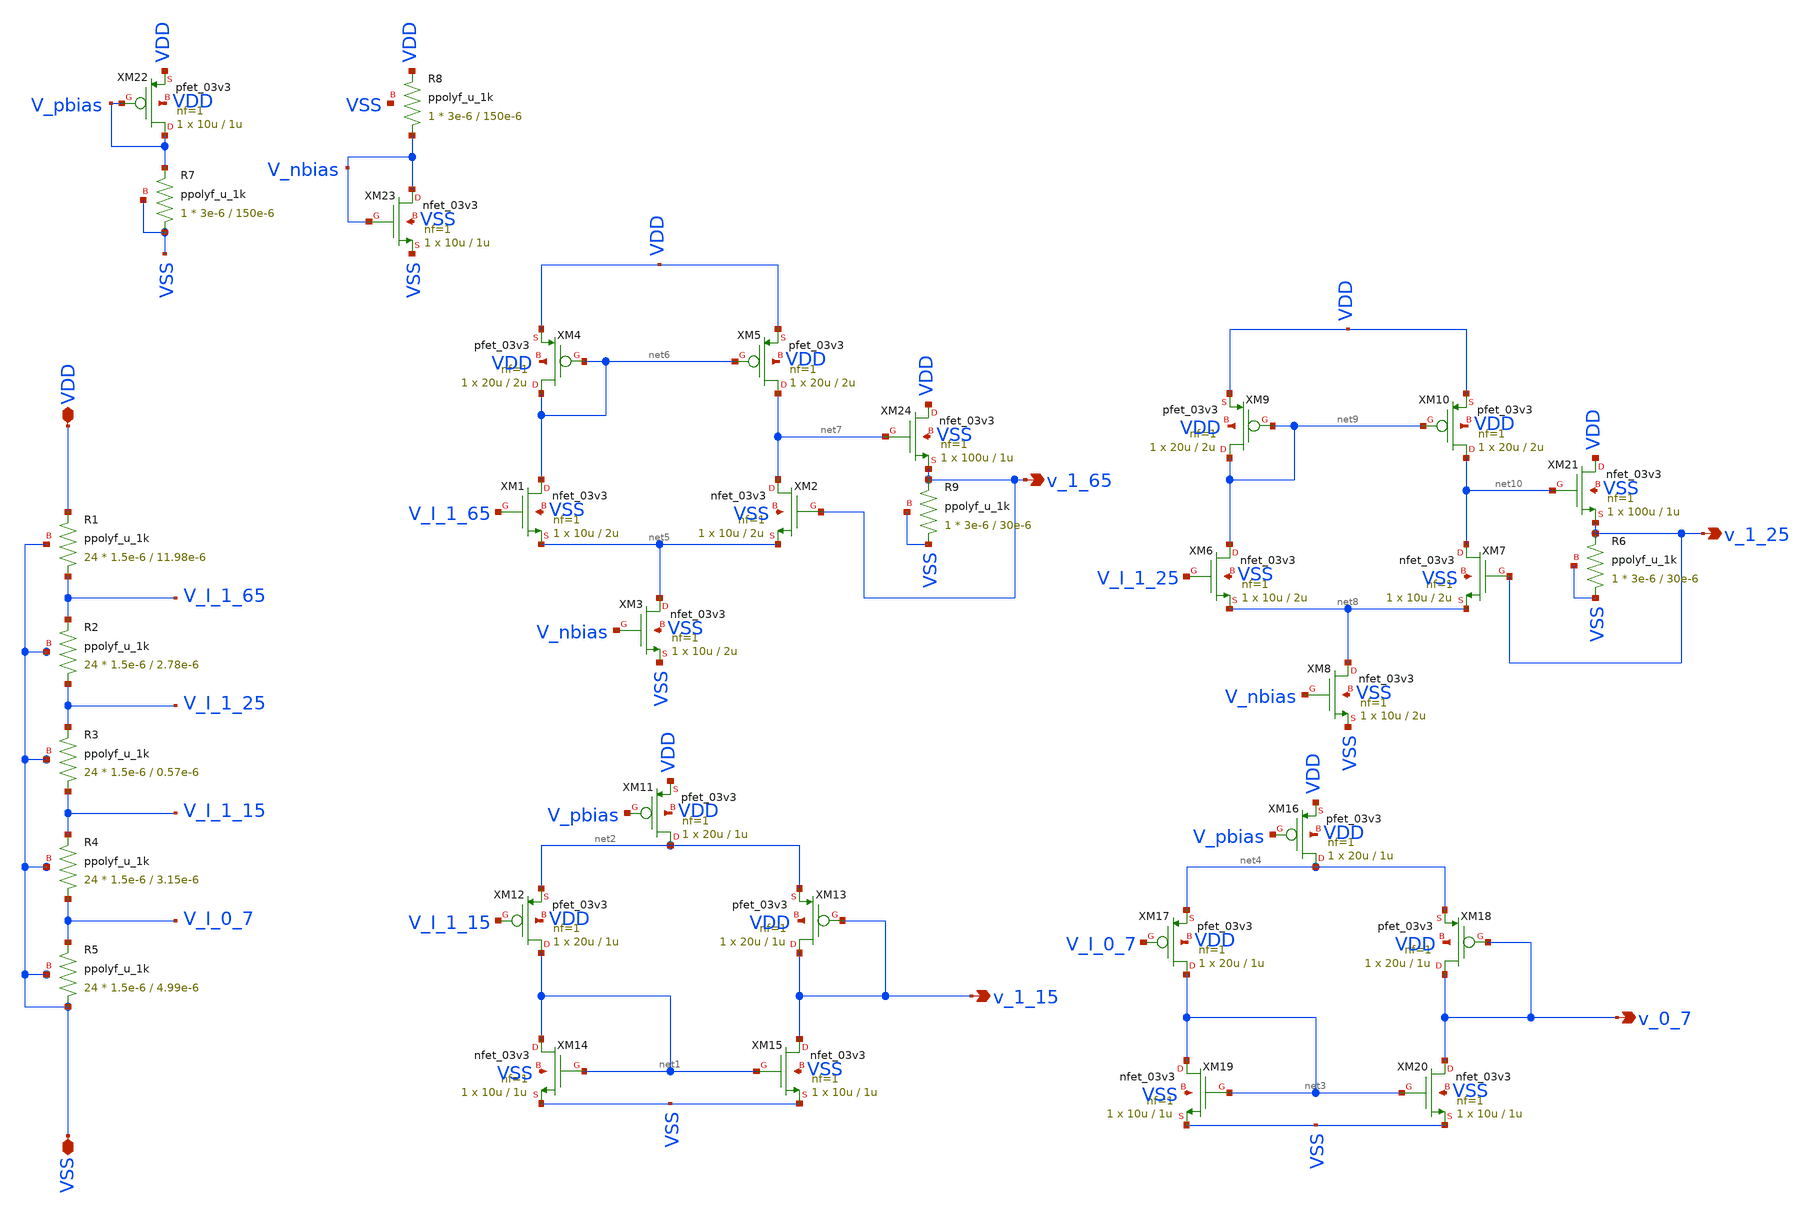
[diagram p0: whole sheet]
** sch_path: schematics/voltage_reference.sch
**.subckt voltage_reference VDD VSS v_1_65 v_1_15 v_0_7 v_1_25
*.iopin VDD
*.iopin VSS
*.opin v_1_65
*.opin v_1_15
*.opin v_0_7
*.opin v_1_25
XR1 V_I_1_65 VDD VSS ppolyf_u_1k r_width=1.5e-6 r_length=11.98e-6 m=24
XR2 V_I_1_25 V_I_1_65 VSS ppolyf_u_1k r_width=1.5e-6 r_length=2.78e-6 m=24
XR3 V_I_1_15 V_I_1_25 VSS ppolyf_u_1k r_width=1.5e-6 r_length=0.57e-6 m=24
XR4 V_I_0_7 V_I_1_15 VSS ppolyf_u_1k r_width=1.5e-6 r_length=3.15e-6 m=24
XR5 VSS V_I_0_7 VSS ppolyf_u_1k r_width=1.5e-6 r_length=4.99e-6 m=24
XM11 net2 V_pbias VDD VDD pfet_03v3 L=1u W=20u nf=1 ad='int((nf+1)/2) * W/nf * 0.18u' as='int((nf+2)/2) * W/nf * 0.18u'
+ pd='2*int((nf+1)/2) * (W/nf + 0.18u)' ps='2*int((nf+2)/2) * (W/nf + 0.18u)' nrd='0.18u / W' nrs='0.18u / W'
+ sa=0 sb=0 sd=0 m=1
XM12 net1 V_I_1_15 net2 VDD pfet_03v3 L=1u W=20u nf=1 ad='int((nf+1)/2) * W/nf * 0.18u' as='int((nf+2)/2) * W/nf * 0.18u'
+ pd='2*int((nf+1)/2) * (W/nf + 0.18u)' ps='2*int((nf+2)/2) * (W/nf + 0.18u)' nrd='0.18u / W' nrs='0.18u / W'
+ sa=0 sb=0 sd=0 m=1
XM13 v_1_15 v_1_15 net2 VDD pfet_03v3 L=1u W=20u nf=1 ad='int((nf+1)/2) * W/nf * 0.18u' as='int((nf+2)/2) * W/nf * 0.18u'
+ pd='2*int((nf+1)/2) * (W/nf + 0.18u)' ps='2*int((nf+2)/2) * (W/nf + 0.18u)' nrd='0.18u / W' nrs='0.18u / W'
+ sa=0 sb=0 sd=0 m=1
XM14 net1 net1 VSS VSS nfet_03v3 L=1u W=10u nf=1 ad='int((nf+1)/2) * W/nf * 0.18u' as='int((nf+2)/2) * W/nf * 0.18u'
+ pd='2*int((nf+1)/2) * (W/nf + 0.18u)' ps='2*int((nf+2)/2) * (W/nf + 0.18u)' nrd='0.18u / W' nrs='0.18u / W'
+ sa=0 sb=0 sd=0 m=1
XM15 v_1_15 net1 VSS VSS nfet_03v3 L=1u W=10u nf=1 ad='int((nf+1)/2) * W/nf * 0.18u' as='int((nf+2)/2) * W/nf * 0.18u'
+ pd='2*int((nf+1)/2) * (W/nf + 0.18u)' ps='2*int((nf+2)/2) * (W/nf + 0.18u)' nrd='0.18u / W' nrs='0.18u / W'
+ sa=0 sb=0 sd=0 m=1
XM16 net4 V_pbias VDD VDD pfet_03v3 L=1u W=20u nf=1 ad='int((nf+1)/2) * W/nf * 0.18u' as='int((nf+2)/2) * W/nf * 0.18u'
+ pd='2*int((nf+1)/2) * (W/nf + 0.18u)' ps='2*int((nf+2)/2) * (W/nf + 0.18u)' nrd='0.18u / W' nrs='0.18u / W'
+ sa=0 sb=0 sd=0 m=1
XM17 net3 V_I_0_7 net4 VDD pfet_03v3 L=1u W=20u nf=1 ad='int((nf+1)/2) * W/nf * 0.18u' as='int((nf+2)/2) * W/nf * 0.18u'
+ pd='2*int((nf+1)/2) * (W/nf + 0.18u)' ps='2*int((nf+2)/2) * (W/nf + 0.18u)' nrd='0.18u / W' nrs='0.18u / W'
+ sa=0 sb=0 sd=0 m=1
XM18 v_0_7 v_0_7 net4 VDD pfet_03v3 L=1u W=20u nf=1 ad='int((nf+1)/2) * W/nf * 0.18u' as='int((nf+2)/2) * W/nf * 0.18u'
+ pd='2*int((nf+1)/2) * (W/nf + 0.18u)' ps='2*int((nf+2)/2) * (W/nf + 0.18u)' nrd='0.18u / W' nrs='0.18u / W'
+ sa=0 sb=0 sd=0 m=1
XM19 net3 net3 VSS VSS nfet_03v3 L=1u W=10u nf=1 ad='int((nf+1)/2) * W/nf * 0.18u' as='int((nf+2)/2) * W/nf * 0.18u'
+ pd='2*int((nf+1)/2) * (W/nf + 0.18u)' ps='2*int((nf+2)/2) * (W/nf + 0.18u)' nrd='0.18u / W' nrs='0.18u / W'
+ sa=0 sb=0 sd=0 m=1
XM20 v_0_7 net3 VSS VSS nfet_03v3 L=1u W=10u nf=1 ad='int((nf+1)/2) * W/nf * 0.18u' as='int((nf+2)/2) * W/nf * 0.18u'
+ pd='2*int((nf+1)/2) * (W/nf + 0.18u)' ps='2*int((nf+2)/2) * (W/nf + 0.18u)' nrd='0.18u / W' nrs='0.18u / W'
+ sa=0 sb=0 sd=0 m=1
XM21 VDD net10 v_1_25 VSS nfet_03v3 L=1u W=100u nf=1 ad='int((nf+1)/2) * W/nf * 0.18u' as='int((nf+2)/2) * W/nf * 0.18u'
+ pd='2*int((nf+1)/2) * (W/nf + 0.18u)' ps='2*int((nf+2)/2) * (W/nf + 0.18u)' nrd='0.18u / W' nrs='0.18u / W'
+ sa=0 sb=0 sd=0 m=1
XR6 VSS v_1_25 VSS ppolyf_u_1k r_width=3e-6 r_length=30e-6 m=1
XM22 V_pbias V_pbias VDD VDD pfet_03v3 L=1u W=10u nf=1 ad='int((nf+1)/2) * W/nf * 0.18u' as='int((nf+2)/2) * W/nf * 0.18u'
+ pd='2*int((nf+1)/2) * (W/nf + 0.18u)' ps='2*int((nf+2)/2) * (W/nf + 0.18u)' nrd='0.18u / W' nrs='0.18u / W'
+ sa=0 sb=0 sd=0 m=1
XR7 VSS V_pbias VSS ppolyf_u_1k r_width=3e-6 r_length=150e-6 m=1
XM1 net6 V_I_1_65 net5 VSS nfet_03v3 L=2u W=10u nf=1 ad='int((nf+1)/2) * W/nf * 0.18u' as='int((nf+2)/2) * W/nf * 0.18u'
+ pd='2*int((nf+1)/2) * (W/nf + 0.18u)' ps='2*int((nf+2)/2) * (W/nf + 0.18u)' nrd='0.18u / W' nrs='0.18u / W'
+ sa=0 sb=0 sd=0 m=1
XM2 net7 v_1_65 net5 VSS nfet_03v3 L=2u W=10u nf=1 ad='int((nf+1)/2) * W/nf * 0.18u' as='int((nf+2)/2) * W/nf * 0.18u'
+ pd='2*int((nf+1)/2) * (W/nf + 0.18u)' ps='2*int((nf+2)/2) * (W/nf + 0.18u)' nrd='0.18u / W' nrs='0.18u / W'
+ sa=0 sb=0 sd=0 m=1
XM3 net5 V_nbias VSS VSS nfet_03v3 L=2u W=10u nf=1 ad='int((nf+1)/2) * W/nf * 0.18u' as='int((nf+2)/2) * W/nf * 0.18u'
+ pd='2*int((nf+1)/2) * (W/nf + 0.18u)' ps='2*int((nf+2)/2) * (W/nf + 0.18u)' nrd='0.18u / W' nrs='0.18u / W'
+ sa=0 sb=0 sd=0 m=1
XM4 net6 net6 VDD VDD pfet_03v3 L=2u W=20u nf=1 ad='int((nf+1)/2) * W/nf * 0.18u' as='int((nf+2)/2) * W/nf * 0.18u'
+ pd='2*int((nf+1)/2) * (W/nf + 0.18u)' ps='2*int((nf+2)/2) * (W/nf + 0.18u)' nrd='0.18u / W' nrs='0.18u / W'
+ sa=0 sb=0 sd=0 m=1
XM5 net7 net6 VDD VDD pfet_03v3 L=2u W=20u nf=1 ad='int((nf+1)/2) * W/nf * 0.18u' as='int((nf+2)/2) * W/nf * 0.18u'
+ pd='2*int((nf+1)/2) * (W/nf + 0.18u)' ps='2*int((nf+2)/2) * (W/nf + 0.18u)' nrd='0.18u / W' nrs='0.18u / W'
+ sa=0 sb=0 sd=0 m=1
XM23 V_nbias V_nbias VSS VSS nfet_03v3 L=1u W=10u nf=1 ad='int((nf+1)/2) * W/nf * 0.18u' as='int((nf+2)/2) * W/nf * 0.18u'
+ pd='2*int((nf+1)/2) * (W/nf + 0.18u)' ps='2*int((nf+2)/2) * (W/nf + 0.18u)' nrd='0.18u / W' nrs='0.18u / W'
+ sa=0 sb=0 sd=0 m=1
XR8 V_nbias VDD VSS ppolyf_u_1k r_width=3e-6 r_length=150e-6 m=1
XM6 net9 V_I_1_25 net8 VSS nfet_03v3 L=2u W=10u nf=1 ad='int((nf+1)/2) * W/nf * 0.18u' as='int((nf+2)/2) * W/nf * 0.18u'
+ pd='2*int((nf+1)/2) * (W/nf + 0.18u)' ps='2*int((nf+2)/2) * (W/nf + 0.18u)' nrd='0.18u / W' nrs='0.18u / W'
+ sa=0 sb=0 sd=0 m=1
XM7 net10 v_1_25 net8 VSS nfet_03v3 L=2u W=10u nf=1 ad='int((nf+1)/2) * W/nf * 0.18u' as='int((nf+2)/2) * W/nf * 0.18u'
+ pd='2*int((nf+1)/2) * (W/nf + 0.18u)' ps='2*int((nf+2)/2) * (W/nf + 0.18u)' nrd='0.18u / W' nrs='0.18u / W'
+ sa=0 sb=0 sd=0 m=1
XM8 net8 V_nbias VSS VSS nfet_03v3 L=2u W=10u nf=1 ad='int((nf+1)/2) * W/nf * 0.18u' as='int((nf+2)/2) * W/nf * 0.18u'
+ pd='2*int((nf+1)/2) * (W/nf + 0.18u)' ps='2*int((nf+2)/2) * (W/nf + 0.18u)' nrd='0.18u / W' nrs='0.18u / W'
+ sa=0 sb=0 sd=0 m=1
XM9 net9 net9 VDD VDD pfet_03v3 L=2u W=20u nf=1 ad='int((nf+1)/2) * W/nf * 0.18u' as='int((nf+2)/2) * W/nf * 0.18u'
+ pd='2*int((nf+1)/2) * (W/nf + 0.18u)' ps='2*int((nf+2)/2) * (W/nf + 0.18u)' nrd='0.18u / W' nrs='0.18u / W'
+ sa=0 sb=0 sd=0 m=1
XM10 net10 net9 VDD VDD pfet_03v3 L=2u W=20u nf=1 ad='int((nf+1)/2) * W/nf * 0.18u' as='int((nf+2)/2) * W/nf * 0.18u'
+ pd='2*int((nf+1)/2) * (W/nf + 0.18u)' ps='2*int((nf+2)/2) * (W/nf + 0.18u)' nrd='0.18u / W' nrs='0.18u / W'
+ sa=0 sb=0 sd=0 m=1
XM24 VDD net7 v_1_65 VSS nfet_03v3 L=1u W=100u nf=1 ad='int((nf+1)/2) * W/nf * 0.18u' as='int((nf+2)/2) * W/nf * 0.18u'
+ pd='2*int((nf+1)/2) * (W/nf + 0.18u)' ps='2*int((nf+2)/2) * (W/nf + 0.18u)' nrd='0.18u / W' nrs='0.18u / W'
+ sa=0 sb=0 sd=0 m=1
XR9 VSS v_1_65 VSS ppolyf_u_1k r_width=3e-6 r_length=30e-6 m=1
**.ends
.end
